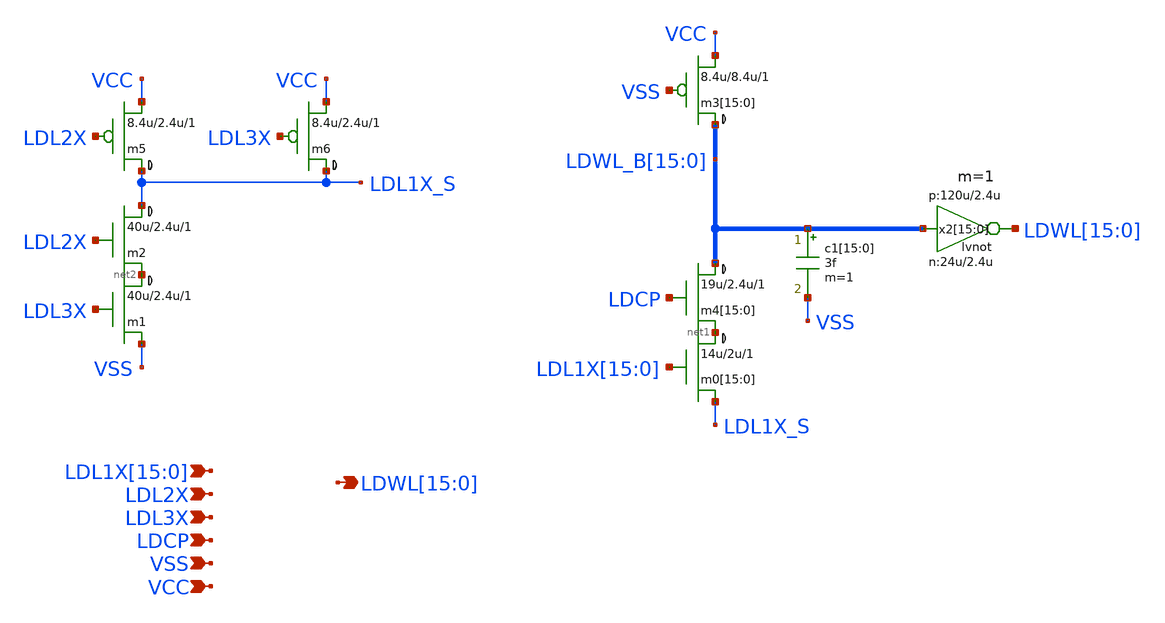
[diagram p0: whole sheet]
** sch_path: xschem-src/xschem_library/rom8k/rom3_rowdec.sch
* Copyright (C) 1998-2026 Stefan Frederik Schippers
* This program is free software; you can redistribute it and/or modify
* it under the terms of the GNU General Public License as published by
* the Free Software Foundation; either version 2 of the License, or
* (at your option) any later version.
* This program is distributed in the hope that it will be useful,
* but WITHOUT ANY WARRANTY; without even the implied warranty of
* MERCHANTABILITY or FITNESS FOR A PARTICULAR PURPOSE.  See the
* GNU General Public License for more details.
* You should have received a copy of the GNU General Public License
* along with this program; if not, write to the Free Software
**.subckt rom3_rowdec
*+ LDWL[15],LDWL[14],LDWL[13],LDWL[12],LDWL[11],LDWL[10],LDWL[9],LDWL[8],LDWL[7],LDWL[6],LDWL[5],LDWL[4],LDWL[3],LDWL[2],LDWL[1],LDWL[0]
*+ LDL1X[15],LDL1X[14],LDL1X[13],LDL1X[12],LDL1X[11],LDL1X[10],LDL1X[9],LDL1X[8],LDL1X[7],LDL1X[6],LDL1X[5],LDL1X[4],LDL1X[3],LDL1X[2],LDL1X[1],LDL1X[0] LDL2X LDL3X LDCP VSS VCC
*.opin
*+ LDWL[15],LDWL[14],LDWL[13],LDWL[12],LDWL[11],LDWL[10],LDWL[9],LDWL[8],LDWL[7],LDWL[6],LDWL[5],LDWL[4],LDWL[3],LDWL[2],LDWL[1],LDWL[0]
*.ipin
*+ LDL1X[15],LDL1X[14],LDL1X[13],LDL1X[12],LDL1X[11],LDL1X[10],LDL1X[9],LDL1X[8],LDL1X[7],LDL1X[6],LDL1X[5],LDL1X[4],LDL1X[3],LDL1X[2],LDL1X[1],LDL1X[0]
*.ipin LDL2X
*.ipin LDL3X
*.ipin LDCP
*.ipin VSS
*.ipin VCC
m0[15] net1[15] LDL1X[15] LDL1X_S 0 cmosn w=14u l=2u ad={14u *4.4u} as={14u *4.4u} pd={14u *2 + 8.8u}
+ ps={14u *2 + 8.8u} m=1
m0[14] net1[14] LDL1X[14] LDL1X_S 0 cmosn w=14u l=2u ad={14u *4.4u} as={14u *4.4u} pd={14u *2 + 8.8u}
+ ps={14u *2 + 8.8u} m=1
m0[13] net1[13] LDL1X[13] LDL1X_S 0 cmosn w=14u l=2u ad={14u *4.4u} as={14u *4.4u} pd={14u *2 + 8.8u}
+ ps={14u *2 + 8.8u} m=1
m0[12] net1[12] LDL1X[12] LDL1X_S 0 cmosn w=14u l=2u ad={14u *4.4u} as={14u *4.4u} pd={14u *2 + 8.8u}
+ ps={14u *2 + 8.8u} m=1
m0[11] net1[11] LDL1X[11] LDL1X_S 0 cmosn w=14u l=2u ad={14u *4.4u} as={14u *4.4u} pd={14u *2 + 8.8u}
+ ps={14u *2 + 8.8u} m=1
m0[10] net1[10] LDL1X[10] LDL1X_S 0 cmosn w=14u l=2u ad={14u *4.4u} as={14u *4.4u} pd={14u *2 + 8.8u}
+ ps={14u *2 + 8.8u} m=1
m0[9] net1[9] LDL1X[9] LDL1X_S 0 cmosn w=14u l=2u ad={14u *4.4u} as={14u *4.4u} pd={14u *2 + 8.8u} ps={14u *2 + 8.8u}
+ m=1
m0[8] net1[8] LDL1X[8] LDL1X_S 0 cmosn w=14u l=2u ad={14u *4.4u} as={14u *4.4u} pd={14u *2 + 8.8u} ps={14u *2 + 8.8u}
+ m=1
m0[7] net1[7] LDL1X[7] LDL1X_S 0 cmosn w=14u l=2u ad={14u *4.4u} as={14u *4.4u} pd={14u *2 + 8.8u} ps={14u *2 + 8.8u}
+ m=1
m0[6] net1[6] LDL1X[6] LDL1X_S 0 cmosn w=14u l=2u ad={14u *4.4u} as={14u *4.4u} pd={14u *2 + 8.8u} ps={14u *2 + 8.8u}
+ m=1
m0[5] net1[5] LDL1X[5] LDL1X_S 0 cmosn w=14u l=2u ad={14u *4.4u} as={14u *4.4u} pd={14u *2 + 8.8u} ps={14u *2 + 8.8u}
+ m=1
m0[4] net1[4] LDL1X[4] LDL1X_S 0 cmosn w=14u l=2u ad={14u *4.4u} as={14u *4.4u} pd={14u *2 + 8.8u} ps={14u *2 + 8.8u}
+ m=1
m0[3] net1[3] LDL1X[3] LDL1X_S 0 cmosn w=14u l=2u ad={14u *4.4u} as={14u *4.4u} pd={14u *2 + 8.8u} ps={14u *2 + 8.8u}
+ m=1
m0[2] net1[2] LDL1X[2] LDL1X_S 0 cmosn w=14u l=2u ad={14u *4.4u} as={14u *4.4u} pd={14u *2 + 8.8u} ps={14u *2 + 8.8u}
+ m=1
m0[1] net1[1] LDL1X[1] LDL1X_S 0 cmosn w=14u l=2u ad={14u *4.4u} as={14u *4.4u} pd={14u *2 + 8.8u} ps={14u *2 + 8.8u}
+ m=1
m0[0] net1[0] LDL1X[0] LDL1X_S 0 cmosn w=14u l=2u ad={14u *4.4u} as={14u *4.4u} pd={14u *2 + 8.8u} ps={14u *2 + 8.8u}
+ m=1
c1[15] LDWL_B[15] VSS 3f m=1
c1[14] LDWL_B[14] VSS 3f m=1
c1[13] LDWL_B[13] VSS 3f m=1
c1[12] LDWL_B[12] VSS 3f m=1
c1[11] LDWL_B[11] VSS 3f m=1
c1[10] LDWL_B[10] VSS 3f m=1
c1[9] LDWL_B[9] VSS 3f m=1
c1[8] LDWL_B[8] VSS 3f m=1
c1[7] LDWL_B[7] VSS 3f m=1
c1[6] LDWL_B[6] VSS 3f m=1
c1[5] LDWL_B[5] VSS 3f m=1
c1[4] LDWL_B[4] VSS 3f m=1
c1[3] LDWL_B[3] VSS 3f m=1
c1[2] LDWL_B[2] VSS 3f m=1
c1[1] LDWL_B[1] VSS 3f m=1
c1[0] LDWL_B[0] VSS 3f m=1
x2[15] LDWL[15] LDWL_B[15] vcc vss lvnot wn=24u lln=2.4u wp=120u lp=2.4u m=1
x2[14] LDWL[14] LDWL_B[14] vcc vss lvnot wn=24u lln=2.4u wp=120u lp=2.4u m=1
x2[13] LDWL[13] LDWL_B[13] vcc vss lvnot wn=24u lln=2.4u wp=120u lp=2.4u m=1
x2[12] LDWL[12] LDWL_B[12] vcc vss lvnot wn=24u lln=2.4u wp=120u lp=2.4u m=1
x2[11] LDWL[11] LDWL_B[11] vcc vss lvnot wn=24u lln=2.4u wp=120u lp=2.4u m=1
x2[10] LDWL[10] LDWL_B[10] vcc vss lvnot wn=24u lln=2.4u wp=120u lp=2.4u m=1
x2[9] LDWL[9] LDWL_B[9] vcc vss lvnot wn=24u lln=2.4u wp=120u lp=2.4u m=1
x2[8] LDWL[8] LDWL_B[8] vcc vss lvnot wn=24u lln=2.4u wp=120u lp=2.4u m=1
x2[7] LDWL[7] LDWL_B[7] vcc vss lvnot wn=24u lln=2.4u wp=120u lp=2.4u m=1
x2[6] LDWL[6] LDWL_B[6] vcc vss lvnot wn=24u lln=2.4u wp=120u lp=2.4u m=1
x2[5] LDWL[5] LDWL_B[5] vcc vss lvnot wn=24u lln=2.4u wp=120u lp=2.4u m=1
x2[4] LDWL[4] LDWL_B[4] vcc vss lvnot wn=24u lln=2.4u wp=120u lp=2.4u m=1
x2[3] LDWL[3] LDWL_B[3] vcc vss lvnot wn=24u lln=2.4u wp=120u lp=2.4u m=1
x2[2] LDWL[2] LDWL_B[2] vcc vss lvnot wn=24u lln=2.4u wp=120u lp=2.4u m=1
x2[1] LDWL[1] LDWL_B[1] vcc vss lvnot wn=24u lln=2.4u wp=120u lp=2.4u m=1
x2[0] LDWL[0] LDWL_B[0] vcc vss lvnot wn=24u lln=2.4u wp=120u lp=2.4u m=1
m3[15] LDWL_B[15] VSS VCC VCC cmosp w=8.4u l=8.4u ad={8.4u *4.4u} as={8.4u *4.4u} pd={8.4u *2 + 8.8u}
+ ps={8.4u *2 + 8.8u} m=1
m3[14] LDWL_B[14] VSS VCC VCC cmosp w=8.4u l=8.4u ad={8.4u *4.4u} as={8.4u *4.4u} pd={8.4u *2 + 8.8u}
+ ps={8.4u *2 + 8.8u} m=1
m3[13] LDWL_B[13] VSS VCC VCC cmosp w=8.4u l=8.4u ad={8.4u *4.4u} as={8.4u *4.4u} pd={8.4u *2 + 8.8u}
+ ps={8.4u *2 + 8.8u} m=1
m3[12] LDWL_B[12] VSS VCC VCC cmosp w=8.4u l=8.4u ad={8.4u *4.4u} as={8.4u *4.4u} pd={8.4u *2 + 8.8u}
+ ps={8.4u *2 + 8.8u} m=1
m3[11] LDWL_B[11] VSS VCC VCC cmosp w=8.4u l=8.4u ad={8.4u *4.4u} as={8.4u *4.4u} pd={8.4u *2 + 8.8u}
+ ps={8.4u *2 + 8.8u} m=1
m3[10] LDWL_B[10] VSS VCC VCC cmosp w=8.4u l=8.4u ad={8.4u *4.4u} as={8.4u *4.4u} pd={8.4u *2 + 8.8u}
+ ps={8.4u *2 + 8.8u} m=1
m3[9] LDWL_B[9] VSS VCC VCC cmosp w=8.4u l=8.4u ad={8.4u *4.4u} as={8.4u *4.4u} pd={8.4u *2 + 8.8u} ps={8.4u *2 + 8.8u}
+ m=1
m3[8] LDWL_B[8] VSS VCC VCC cmosp w=8.4u l=8.4u ad={8.4u *4.4u} as={8.4u *4.4u} pd={8.4u *2 + 8.8u} ps={8.4u *2 + 8.8u}
+ m=1
m3[7] LDWL_B[7] VSS VCC VCC cmosp w=8.4u l=8.4u ad={8.4u *4.4u} as={8.4u *4.4u} pd={8.4u *2 + 8.8u} ps={8.4u *2 + 8.8u}
+ m=1
m3[6] LDWL_B[6] VSS VCC VCC cmosp w=8.4u l=8.4u ad={8.4u *4.4u} as={8.4u *4.4u} pd={8.4u *2 + 8.8u} ps={8.4u *2 + 8.8u}
+ m=1
m3[5] LDWL_B[5] VSS VCC VCC cmosp w=8.4u l=8.4u ad={8.4u *4.4u} as={8.4u *4.4u} pd={8.4u *2 + 8.8u} ps={8.4u *2 + 8.8u}
+ m=1
m3[4] LDWL_B[4] VSS VCC VCC cmosp w=8.4u l=8.4u ad={8.4u *4.4u} as={8.4u *4.4u} pd={8.4u *2 + 8.8u} ps={8.4u *2 + 8.8u}
+ m=1
m3[3] LDWL_B[3] VSS VCC VCC cmosp w=8.4u l=8.4u ad={8.4u *4.4u} as={8.4u *4.4u} pd={8.4u *2 + 8.8u} ps={8.4u *2 + 8.8u}
+ m=1
m3[2] LDWL_B[2] VSS VCC VCC cmosp w=8.4u l=8.4u ad={8.4u *4.4u} as={8.4u *4.4u} pd={8.4u *2 + 8.8u} ps={8.4u *2 + 8.8u}
+ m=1
m3[1] LDWL_B[1] VSS VCC VCC cmosp w=8.4u l=8.4u ad={8.4u *4.4u} as={8.4u *4.4u} pd={8.4u *2 + 8.8u} ps={8.4u *2 + 8.8u}
+ m=1
m3[0] LDWL_B[0] VSS VCC VCC cmosp w=8.4u l=8.4u ad={8.4u *4.4u} as={8.4u *4.4u} pd={8.4u *2 + 8.8u} ps={8.4u *2 + 8.8u}
+ m=1
m4[15] LDWL_B[15] LDCP net1[15] 0 cmosn w=19u l=2.4u ad={19u *4.4u} as={19u *4.4u} pd={19u *2 + 8.8u}
+ ps={19u *2 + 8.8u} m=1
m4[14] LDWL_B[14] LDCP net1[14] 0 cmosn w=19u l=2.4u ad={19u *4.4u} as={19u *4.4u} pd={19u *2 + 8.8u}
+ ps={19u *2 + 8.8u} m=1
m4[13] LDWL_B[13] LDCP net1[13] 0 cmosn w=19u l=2.4u ad={19u *4.4u} as={19u *4.4u} pd={19u *2 + 8.8u}
+ ps={19u *2 + 8.8u} m=1
m4[12] LDWL_B[12] LDCP net1[12] 0 cmosn w=19u l=2.4u ad={19u *4.4u} as={19u *4.4u} pd={19u *2 + 8.8u}
+ ps={19u *2 + 8.8u} m=1
m4[11] LDWL_B[11] LDCP net1[11] 0 cmosn w=19u l=2.4u ad={19u *4.4u} as={19u *4.4u} pd={19u *2 + 8.8u}
+ ps={19u *2 + 8.8u} m=1
m4[10] LDWL_B[10] LDCP net1[10] 0 cmosn w=19u l=2.4u ad={19u *4.4u} as={19u *4.4u} pd={19u *2 + 8.8u}
+ ps={19u *2 + 8.8u} m=1
m4[9] LDWL_B[9] LDCP net1[9] 0 cmosn w=19u l=2.4u ad={19u *4.4u} as={19u *4.4u} pd={19u *2 + 8.8u} ps={19u *2 + 8.8u}
+ m=1
m4[8] LDWL_B[8] LDCP net1[8] 0 cmosn w=19u l=2.4u ad={19u *4.4u} as={19u *4.4u} pd={19u *2 + 8.8u} ps={19u *2 + 8.8u}
+ m=1
m4[7] LDWL_B[7] LDCP net1[7] 0 cmosn w=19u l=2.4u ad={19u *4.4u} as={19u *4.4u} pd={19u *2 + 8.8u} ps={19u *2 + 8.8u}
+ m=1
m4[6] LDWL_B[6] LDCP net1[6] 0 cmosn w=19u l=2.4u ad={19u *4.4u} as={19u *4.4u} pd={19u *2 + 8.8u} ps={19u *2 + 8.8u}
+ m=1
m4[5] LDWL_B[5] LDCP net1[5] 0 cmosn w=19u l=2.4u ad={19u *4.4u} as={19u *4.4u} pd={19u *2 + 8.8u} ps={19u *2 + 8.8u}
+ m=1
m4[4] LDWL_B[4] LDCP net1[4] 0 cmosn w=19u l=2.4u ad={19u *4.4u} as={19u *4.4u} pd={19u *2 + 8.8u} ps={19u *2 + 8.8u}
+ m=1
m4[3] LDWL_B[3] LDCP net1[3] 0 cmosn w=19u l=2.4u ad={19u *4.4u} as={19u *4.4u} pd={19u *2 + 8.8u} ps={19u *2 + 8.8u}
+ m=1
m4[2] LDWL_B[2] LDCP net1[2] 0 cmosn w=19u l=2.4u ad={19u *4.4u} as={19u *4.4u} pd={19u *2 + 8.8u} ps={19u *2 + 8.8u}
+ m=1
m4[1] LDWL_B[1] LDCP net1[1] 0 cmosn w=19u l=2.4u ad={19u *4.4u} as={19u *4.4u} pd={19u *2 + 8.8u} ps={19u *2 + 8.8u}
+ m=1
m4[0] LDWL_B[0] LDCP net1[0] 0 cmosn w=19u l=2.4u ad={19u *4.4u} as={19u *4.4u} pd={19u *2 + 8.8u} ps={19u *2 + 8.8u}
+ m=1
m1 net2 LDL3X VSS 0 cmosn w=40u l=2.4u ad={40u *4.4u} as={40u *4.4u} pd={40u *2 + 8.8u} ps={40u *2 + 8.8u}
+ m=1
m2 LDL1X_S LDL2X net2 0 cmosn w=40u l=2.4u ad={40u *4.4u} as={40u *4.4u} pd={40u *2 + 8.8u} ps={40u *2 + 8.8u}
+ m=1
m5 LDL1X_S LDL2X VCC VCC cmosp w=8.4u l=2.4u ad={8.4u *4.4u} as={8.4u *4.4u} pd={8.4u *2 + 8.8u} ps={8.4u *2 + 8.8u}
+ m=1
m6 LDL1X_S LDL3X VCC VCC cmosp w=8.4u l=2.4u ad={8.4u *4.4u} as={8.4u *4.4u} pd={8.4u *2 + 8.8u} ps={8.4u *2 + 8.8u}
+ m=1
**.ends

* expanding   symbol:  lvnot.sym # of pins=2
** sym_path: xschem-src/xschem_library/rom8k/lvnot.sym
** sch_path: xschem-src/xschem_library/rom8k/lvnot.sch
.subckt lvnot y a VCCPIN VSSPIN     wn=10u lln=1.2u wp=10u lp=1.2u
*.opin y
*.ipin a
m2 DP a VCCPIN VCCPIN cmosp w=wp l=lp ad='wp *4.6u' as='wp *4.6u' pd='wp *2+9.2u' ps='wp *2+9.2u' m=1
m1 DN a VSSPIN VSSPIN cmosn w=wn l=lln ad='wn *4.3u' as='wn *4.3u' pd='wn *2+8.6u' ps='wn *2+8.6u' m=1
Vmeas DP y 0
.save i(vmeas)
Vmeas1 y DN 0
.save i(vmeas1)
.save v(dp)
.save v(dn)
.ends

.end
